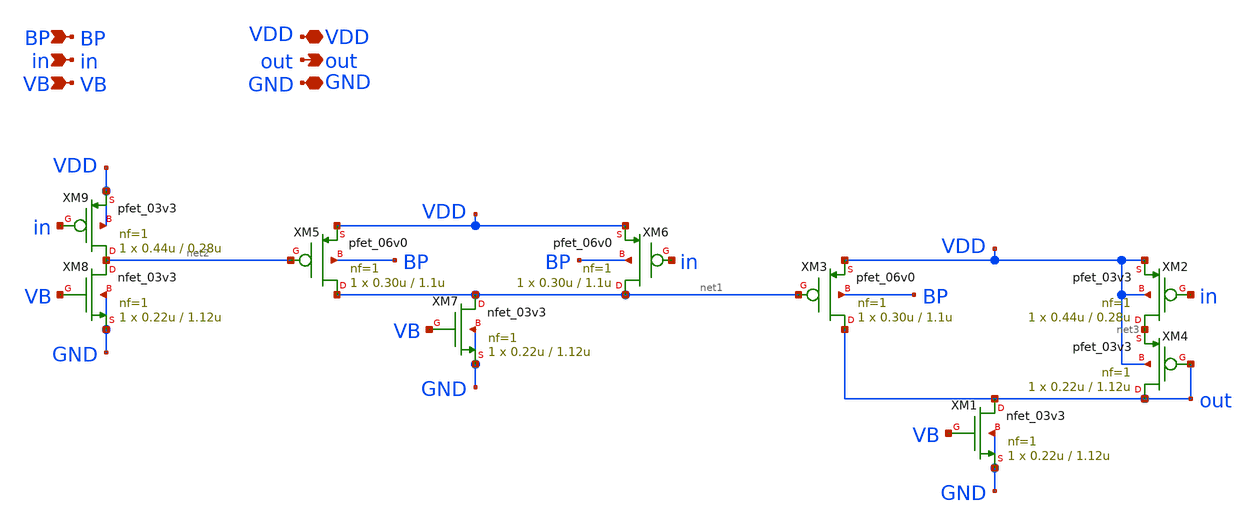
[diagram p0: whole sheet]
** sch_path: xschem_sn2/cyc_up.sch
**.subckt cyc_up in GND VDD BP VB out
*.ipin in
*.iopin GND
*.iopin VDD
*.ipin BP
*.ipin VB
*.opin out
XM2 net3 in VDD VDD pfet_03v3 L=0.28u W=0.44u nf=1 ad='int((nf+1)/2) * W/nf * 0.18u' as='int((nf+2)/2) * W/nf * 0.18u'
+ pd='2*int((nf+1)/2) * (W/nf + 0.18u)' ps='2*int((nf+2)/2) * (W/nf + 0.18u)' nrd='0.18u / W' nrs='0.18u / W'
+ sa=0 sb=0 sd=0 m=1 par=1
XM3 out net1 VDD BP pfet_06v0 L=1.1u W=0.30u nf=1 ad='int((nf+1)/2) * W/nf * 0.18u' as='int((nf+2)/2) * W/nf * 0.18u'
+ pd='2*int((nf+1)/2) * (W/nf + 0.18u)' ps='2*int((nf+2)/2) * (W/nf + 0.18u)' nrd='0.18u / W' nrs='0.18u / W'
+ sa=0 sb=0 sd=0 m=1
XM4 out out net3 VDD pfet_03v3 L=1.12u W=0.22u nf=1 ad='int((nf+1)/2) * W/nf * 0.18u' as='int((nf+2)/2) * W/nf * 0.18u'
+ pd='2*int((nf+1)/2) * (W/nf + 0.18u)' ps='2*int((nf+2)/2) * (W/nf + 0.18u)' nrd='0.18u / W' nrs='0.18u / W'
+ sa=0 sb=0 sd=0 m=1 par=1
XM8 net2 VB GND GND nfet_03v3 L=1.12u W=0.22u nf=1 ad='int((nf+1)/2) * W/nf * 0.18u' as='int((nf+2)/2) * W/nf * 0.18u'
+ pd='2*int((nf+1)/2) * (W/nf + 0.18u)' ps='2*int((nf+2)/2) * (W/nf + 0.18u)' nrd='0.18u / W' nrs='0.18u / W'
+ sa=0 sb=0 sd=0 m=1 par=1
XM9 net2 in VDD VDD pfet_03v3 L=0.28u W=0.44u nf=1 ad='int((nf+1)/2) * W/nf * 0.18u' as='int((nf+2)/2) * W/nf * 0.18u'
+ pd='2*int((nf+1)/2) * (W/nf + 0.18u)' ps='2*int((nf+2)/2) * (W/nf + 0.18u)' nrd='0.18u / W' nrs='0.18u / W'
+ sa=0 sb=0 sd=0 m=1 par=1
XM7 net1 VB GND GND nfet_03v3 L=1.12u W=0.22u nf=1 ad='int((nf+1)/2) * W/nf * 0.18u' as='int((nf+2)/2) * W/nf * 0.18u'
+ pd='2*int((nf+1)/2) * (W/nf + 0.18u)' ps='2*int((nf+2)/2) * (W/nf + 0.18u)' nrd='0.18u / W' nrs='0.18u / W'
+ sa=0 sb=0 sd=0 m=1 par=1
XM1 out VB GND GND nfet_03v3 L=1.12u W=0.22u nf=1 ad='int((nf+1)/2) * W/nf * 0.18u' as='int((nf+2)/2) * W/nf * 0.18u'
+ pd='2*int((nf+1)/2) * (W/nf + 0.18u)' ps='2*int((nf+2)/2) * (W/nf + 0.18u)' nrd='0.18u / W' nrs='0.18u / W'
+ sa=0 sb=0 sd=0 m=1 par=1
XM5 net1 net2 VDD BP pfet_06v0 L=1.1u W=0.30u nf=1 ad='int((nf+1)/2) * W/nf * 0.18u' as='int((nf+2)/2) * W/nf * 0.18u'
+ pd='2*int((nf+1)/2) * (W/nf + 0.18u)' ps='2*int((nf+2)/2) * (W/nf + 0.18u)' nrd='0.18u / W' nrs='0.18u / W'
+ sa=0 sb=0 sd=0 m=1
XM6 net1 in VDD BP pfet_06v0 L=1.1u W=0.30u nf=1 ad='int((nf+1)/2) * W/nf * 0.18u' as='int((nf+2)/2) * W/nf * 0.18u'
+ pd='2*int((nf+1)/2) * (W/nf + 0.18u)' ps='2*int((nf+2)/2) * (W/nf + 0.18u)' nrd='0.18u / W' nrs='0.18u / W'
+ sa=0 sb=0 sd=0 m=1
**.ends
.end
